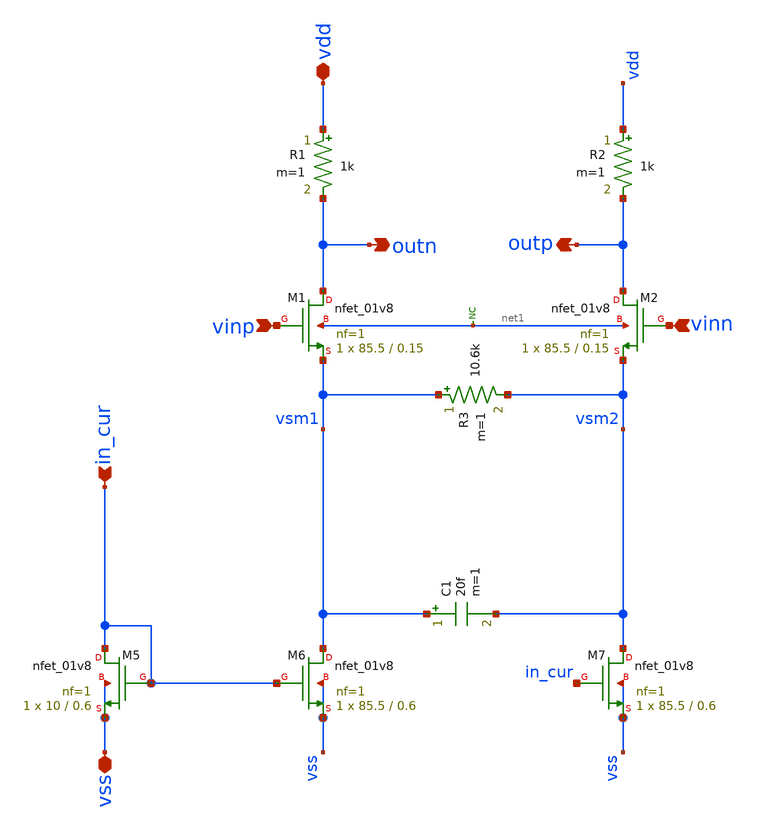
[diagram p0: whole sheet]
** sch_path: CTLE/Old_Design/ctle-base.sch
**.subckt ctle-base vdd vss vinp vinn outn outp in_cur
*.iopin vdd
*.iopin vss
*.ipin vinp
*.ipin vinn
*.opin outn
*.opin outp
*.ipin in_cur
XM1 outn vinp vsm1 net1 sky130_fd_pr__nfet_01v8 L=0.15 W=85.5 nf=1 ad='int((nf+1)/2) * W/nf * 0.29' as='int((nf+2)/2) * W/nf * 0.29'
+ pd='2*int((nf+1)/2) * (W/nf + 0.29)' ps='2*int((nf+2)/2) * (W/nf + 0.29)' nrd='0.29 / W' nrs='0.29 / W'
+ sa=0 sb=0 sd=0 mult=1 m=1
XM2 outp vinn vsm2 net1 sky130_fd_pr__nfet_01v8 L=0.15 W=85.5 nf=1 ad='int((nf+1)/2) * W/nf * 0.29' as='int((nf+2)/2) * W/nf * 0.29'
+ pd='2*int((nf+1)/2) * (W/nf + 0.29)' ps='2*int((nf+2)/2) * (W/nf + 0.29)' nrd='0.29 / W' nrs='0.29 / W'
+ sa=0 sb=0 sd=0 mult=1 m=1
XM5 in_cur in_cur vss vss sky130_fd_pr__nfet_01v8 L=0.6 W=10 nf=1 ad='int((nf+1)/2) * W/nf * 0.29' as='int((nf+2)/2) * W/nf * 0.29'
+ pd='2*int((nf+1)/2) * (W/nf + 0.29)' ps='2*int((nf+2)/2) * (W/nf + 0.29)' nrd='0.29 / W' nrs='0.29 / W'
+ sa=0 sb=0 sd=0 mult=1 m=1
XM6 vsm1 in_cur vss vss sky130_fd_pr__nfet_01v8 L=0.6 W=85.5 nf=1 ad='int((nf+1)/2) * W/nf * 0.29' as='int((nf+2)/2) * W/nf * 0.29'
+ pd='2*int((nf+1)/2) * (W/nf + 0.29)' ps='2*int((nf+2)/2) * (W/nf + 0.29)' nrd='0.29 / W' nrs='0.29 / W'
+ sa=0 sb=0 sd=0 mult=1 m=1
XM7 vsm2 in_cur vss vss sky130_fd_pr__nfet_01v8 L=0.6 W=85.5 nf=1 ad='int((nf+1)/2) * W/nf * 0.29' as='int((nf+2)/2) * W/nf * 0.29'
+ pd='2*int((nf+1)/2) * (W/nf + 0.29)' ps='2*int((nf+2)/2) * (W/nf + 0.29)' nrd='0.29 / W' nrs='0.29 / W'
+ sa=0 sb=0 sd=0 mult=1 m=1
C1 vsm1 vsm2 20f m=1
R3 vsm1 vsm2 10.6k m=1
R1 vdd outn 1k m=1
R2 vdd outp 1k m=1
* noconn #net1
**.ends
.end
